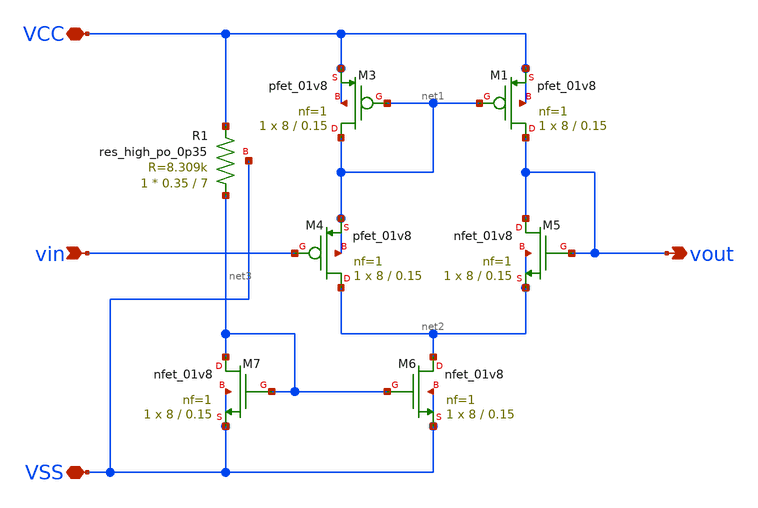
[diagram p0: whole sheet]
** sch_path: xschem/vbuff.sch
**.subckt vbuff VCC VSS vin vout
*.iopin VCC
*.iopin VSS
*.ipin vin
*.opin vout
XM1 vout net1 VCC VCC sky130_fd_pr__pfet_01v8 L=0.15 W=8 nf=1 ad='int((nf+1)/2) * W/nf * 0.29' as='int((nf+2)/2) * W/nf * 0.29'
+ pd='2*int((nf+1)/2) * (W/nf + 0.29)' ps='2*int((nf+2)/2) * (W/nf + 0.29)' nrd='0.29 / W' nrs='0.29 / W'
+ sa=0 sb=0 sd=0 mult=1 m=1
XM3 net1 net1 VCC VCC sky130_fd_pr__pfet_01v8 L=0.15 W=8 nf=1 ad='int((nf+1)/2) * W/nf * 0.29' as='int((nf+2)/2) * W/nf * 0.29'
+ pd='2*int((nf+1)/2) * (W/nf + 0.29)' ps='2*int((nf+2)/2) * (W/nf + 0.29)' nrd='0.29 / W' nrs='0.29 / W'
+ sa=0 sb=0 sd=0 mult=1 m=1
XM4 net2 vin net1 net1 sky130_fd_pr__pfet_01v8 L=0.15 W=8 nf=1 ad='int((nf+1)/2) * W/nf * 0.29' as='int((nf+2)/2) * W/nf * 0.29'
+ pd='2*int((nf+1)/2) * (W/nf + 0.29)' ps='2*int((nf+2)/2) * (W/nf + 0.29)' nrd='0.29 / W' nrs='0.29 / W'
+ sa=0 sb=0 sd=0 mult=1 m=1
XM5 vout vout net2 net2 sky130_fd_pr__nfet_01v8 L=0.15 W=8 nf=1 ad='int((nf+1)/2) * W/nf * 0.29' as='int((nf+2)/2) * W/nf * 0.29'
+ pd='2*int((nf+1)/2) * (W/nf + 0.29)' ps='2*int((nf+2)/2) * (W/nf + 0.29)' nrd='0.29 / W' nrs='0.29 / W'
+ sa=0 sb=0 sd=0 mult=1 m=1
XM6 net2 net3 VSS VSS sky130_fd_pr__nfet_01v8 L=0.15 W=8 nf=1 ad='int((nf+1)/2) * W/nf * 0.29' as='int((nf+2)/2) * W/nf * 0.29'
+ pd='2*int((nf+1)/2) * (W/nf + 0.29)' ps='2*int((nf+2)/2) * (W/nf + 0.29)' nrd='0.29 / W' nrs='0.29 / W'
+ sa=0 sb=0 sd=0 mult=1 m=1
XM7 net3 net3 VSS VSS sky130_fd_pr__nfet_01v8 L=0.15 W=8 nf=1 ad='int((nf+1)/2) * W/nf * 0.29' as='int((nf+2)/2) * W/nf * 0.29'
+ pd='2*int((nf+1)/2) * (W/nf + 0.29)' ps='2*int((nf+2)/2) * (W/nf + 0.29)' nrd='0.29 / W' nrs='0.29 / W'
+ sa=0 sb=0 sd=0 mult=1 m=1
XR1 net3 VCC VSS sky130_fd_pr__res_high_po_0p35 L=7 mult=1 m=1
**.ends
.end
